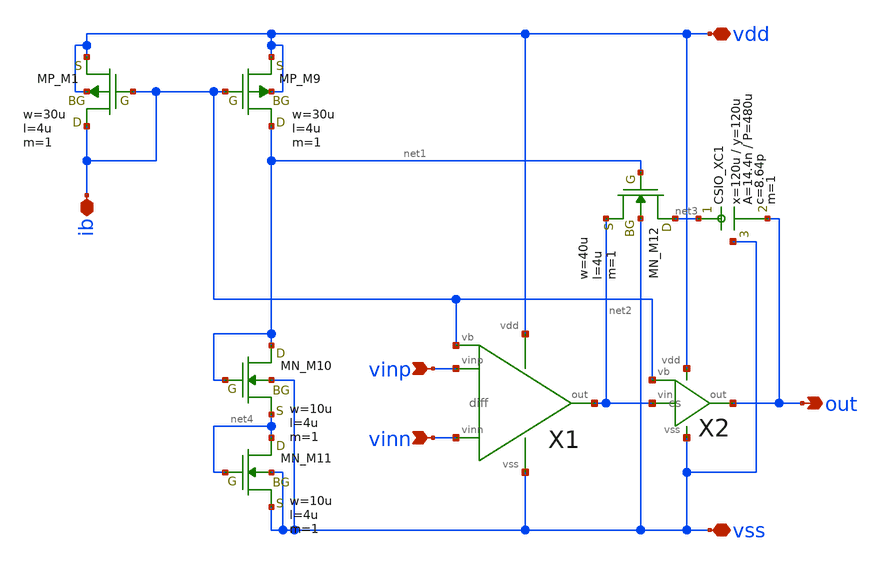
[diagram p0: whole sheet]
** sch_path: member_project/opamp/july_fifth/opamp_july_fifth.sch
**.subckt opamp_july_fifth vinp vinn out vdd vss ib
*.ipin vinp
*.ipin vinn
*.opin out
*.iopin vdd
*.iopin vss
*.iopin ib
X1 vinp vinn net2 vdd vss ib diff
X2 net2 ib out vdd vss cs
XM9 net1 ib vdd vdd PMOS w=30u l=4u as=0 ad=0 ps=0 pd=0 nrd=0 nrs=0 m=1
XM12 net3 net1 net2 vss NMOS w=40u l=4u as=0 ad=0 ps=0 pd=0 nrd=0 nrs=0 m=1
XM1 ib ib vdd vdd PMOS w=30u l=4u as=0 ad=0 ps=0 pd=0 nrd=0 nrs=0 m=1
XM10 net1 net1 net4 vss NMOS w=10u l=4u as=0 ad=0 ps=0 pd=0 nrd=0 nrs=0 m=1
XM11 net4 net4 vss vss NMOS w=10u l=4u as=0 ad=0 ps=0 pd=0 nrd=0 nrs=0 m=1
XXC1 net3 out vss F_CSIO c=8.64p x=120u y=120u m=1
**.ends

* expanding   symbol:  diff.sym # of pins=6
** sym_path: diff.sym
** sch_path: diff.sch
.subckt diff vinp vinn out vdd vss vb
*.ipin vinn
*.ipin vinp
*.ipin vb
*.opin out
*.iopin vdd
*.iopin vss
XM5 net2 vb vdd vdd PMOS w=160u l=4u as=0 ad=0 ps=0 pd=0 nrd=0 nrs=0 m=1
XM1 net1 vinn net2 net2 PMOS w=360u l=4u as=0 ad=0 ps=0 pd=0 nrd=0 nrs=0 m=1
XM2 out vinp net2 net2 PMOS w=360u l=4u as=0 ad=0 ps=0 pd=0 nrd=0 nrs=0 m=1
XM3 net1 net1 vss vss NMOS w=40u l=4u as=0 ad=0 ps=0 pd=0 nrd=0 nrs=0 m=1
XM4 out net1 vss vss NMOS w=40u l=4u as=0 ad=0 ps=0 pd=0 nrd=0 nrs=0 m=1
.ends


* expanding   symbol:  cs.sym # of pins=5
** sym_path: cs.sym
** sch_path: cs.sch
.subckt cs vin vb out vdd vss
*.ipin vb
*.ipin vin
*.opin out
*.iopin vss
*.iopin vdd
XM6 out vb vdd vdd PMOS w=400u l=4u as=0 ad=0 ps=0 pd=0 nrd=0 nrs=0 m=1
XM7 out vin vss vss NMOS w=200u l=4u as=0 ad=0 ps=0 pd=0 nrd=0 nrs=0 m=1
.ends

.end
